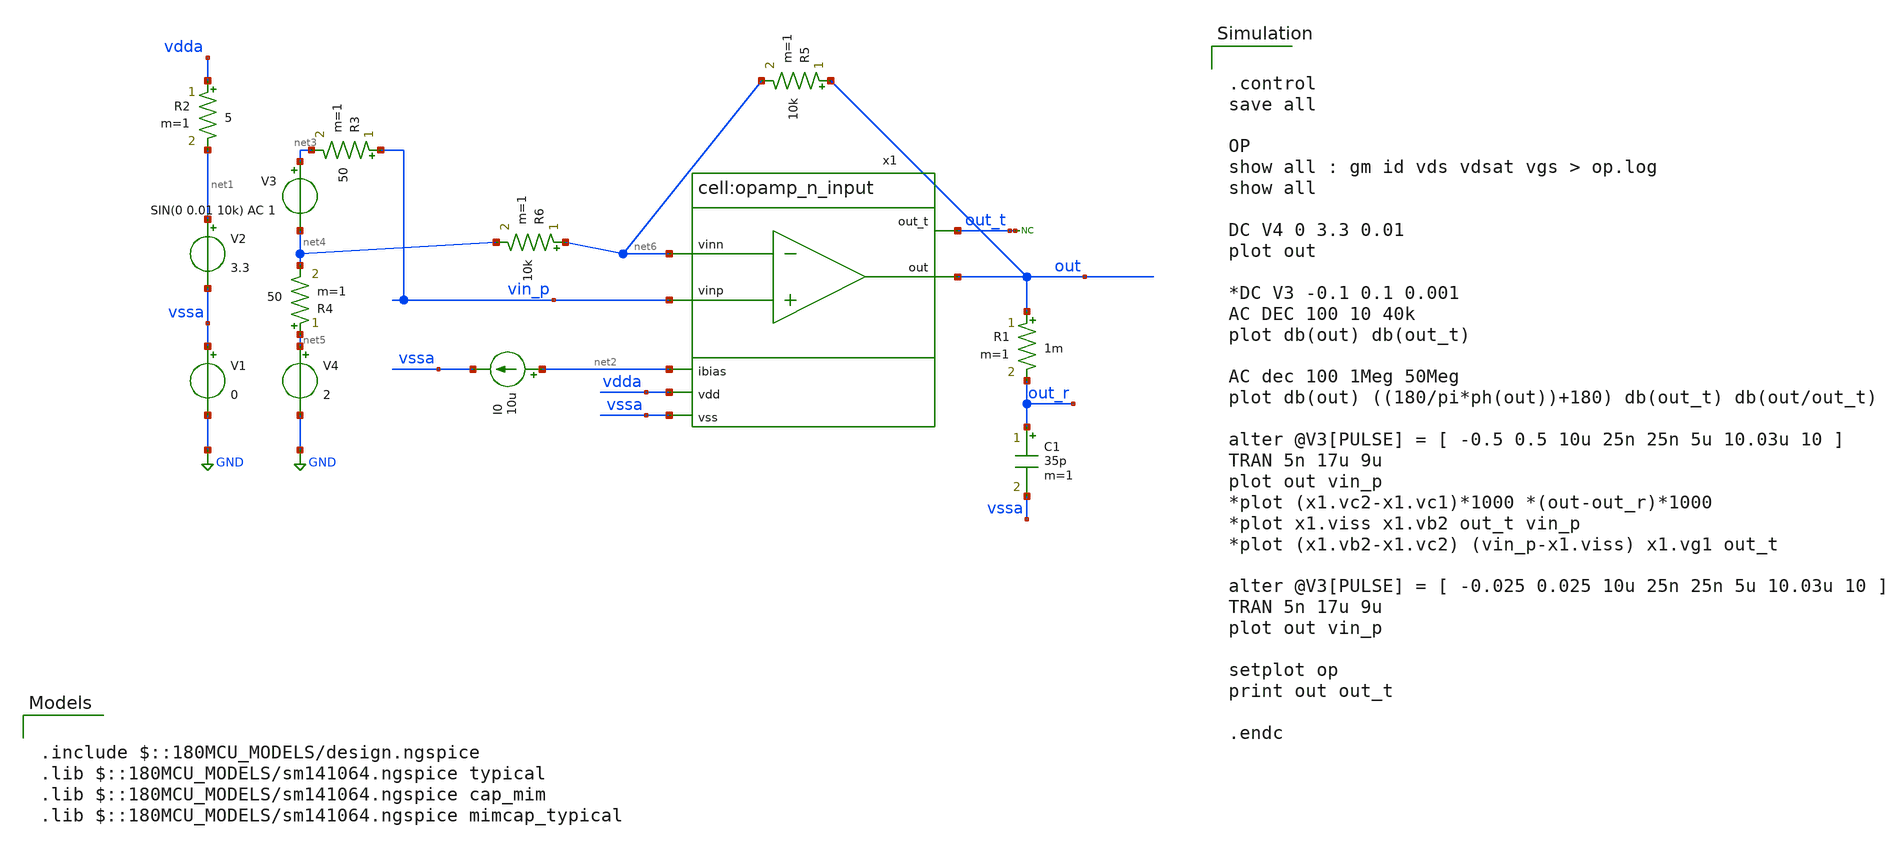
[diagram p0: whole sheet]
** sch_path: designs/libs/tb_analog/opamp/opamp_n_tb.sch
**.subckt opamp_n_tb
x1 vin_p net6 net2 vdda out vssa out_t opamp_n_input
V1 vssa GND 0
V2 net1 vssa 3.3
I0 net2 vssa 10u
V3 net3 net4 SIN(0 0.01 10k) AC 1
V4 net5 GND 2
C1 out_r vssa 35p m=1
* noconn out_t
R1 out out_r 1m m=1
R2 vdda net1 5 m=1
R3 vin_p net3 50 m=1
R4 net5 net4 50 m=1
R5 out net6 10k m=1
R6 net6 net4 10k m=1
**** begin user architecture code


.control
save all

OP
show all : gm id vds vdsat vgs > op.log
show all

DC V4 0 3.3 0.01
plot out

*DC V3 -0.1 0.1 0.001
AC DEC 100 10 40k
plot db(out) db(out_t)

AC dec 100 1Meg 50Meg
plot db(out) ((180/pi*ph(out))+180) db(out_t) db(out/out_t)

alter @V3[PULSE] = [ -0.5 0.5 10u 25n 25n 5u 10.03u 10 ]
TRAN 5n 17u 9u
plot out vin_p
*plot (x1.vc2-x1.vc1)*1000 *(out-out_r)*1000
*plot x1.viss x1.vb2 out_t vin_p
*plot (x1.vb2-x1.vc2) (vin_p-x1.viss) x1.vg1 out_t

alter @V3[PULSE] = [ -0.025 0.025 10u 25n 25n 5u 10.03u 10 ]
TRAN 5n 17u 9u
plot out vin_p

setplot op
print out out_t

.endc



.include $::180MCU_MODELS/design.ngspice
.lib $::180MCU_MODELS/sm141064.ngspice typical
.lib $::180MCU_MODELS/sm141064.ngspice cap_mim
.lib $::180MCU_MODELS/sm141064.ngspice mimcap_typical

**** end user architecture code
**.ends

* expanding   symbol:  libs/core_analog/opamp/opamp_n_input.sym # of pins=7
** sym_path: designs/libs/core_analog/opamp/opamp_n_input.sym
** sch_path: designs/libs/core_analog/opamp/opamp_n_input.sch
.subckt opamp_n_input vinp vinn ibias vdd out vss out_t
*.opin out
*.ipin vdd
*.ipin vss
*.ipin vinn
*.ipin ibias
*.ipin vinp
*.opin out_t
XM1 net1 vinn viss vss nfet_03v3 L=1u W=3u nf=1 ad='int((nf+1)/2) * W/nf * 0.18u' as='int((nf+2)/2) * W/nf * 0.18u'
+ pd='2*int((nf+1)/2) * (W/nf + 0.18u)' ps='2*int((nf+2)/2) * (W/nf + 0.18u)' nrd='0.18u / W' nrs='0.18u / W'
+ sa=0 sb=0 sd=0 m=1
XM2 net2 vinp viss vss nfet_03v3 L=1u W=3u nf=1 ad='int((nf+1)/2) * W/nf * 0.18u' as='int((nf+2)/2) * W/nf * 0.18u'
+ pd='2*int((nf+1)/2) * (W/nf + 0.18u)' ps='2*int((nf+2)/2) * (W/nf + 0.18u)' nrd='0.18u / W' nrs='0.18u / W'
+ sa=0 sb=0 sd=0 m=1
XM6 out_t vg1 vdd vdd pfet_03v3 L=1u W=5u nf=1 ad='int((nf+1)/2) * W/nf * 0.18u' as='int((nf+2)/2) * W/nf * 0.18u'
+ pd='2*int((nf+1)/2) * (W/nf + 0.18u)' ps='2*int((nf+2)/2) * (W/nf + 0.18u)' nrd='0.18u / W' nrs='0.18u / W'
+ sa=0 sb=0 sd=0 m=3
XM5 vg1 vg1 vdd vdd pfet_03v3 L=1u W=5u nf=1 ad='int((nf+1)/2) * W/nf * 0.18u' as='int((nf+2)/2) * W/nf * 0.18u'
+ pd='2*int((nf+1)/2) * (W/nf + 0.18u)' ps='2*int((nf+2)/2) * (W/nf + 0.18u)' nrd='0.18u / W' nrs='0.18u / W'
+ sa=0 sb=0 sd=0 m=3
XM4 out_t vb2 net2 vss nfet_03v3 L=0.6u W=5u nf=1 ad='int((nf+1)/2) * W/nf * 0.18u' as='int((nf+2)/2) * W/nf * 0.18u'
+ pd='2*int((nf+1)/2) * (W/nf + 0.18u)' ps='2*int((nf+2)/2) * (W/nf + 0.18u)' nrd='0.18u / W' nrs='0.18u / W'
+ sa=0 sb=0 sd=0 m=4
XM3 vg1 vb2 net1 vss nfet_03v3 L=0.6u W=5u nf=1 ad='int((nf+1)/2) * W/nf * 0.18u' as='int((nf+2)/2) * W/nf * 0.18u'
+ pd='2*int((nf+1)/2) * (W/nf + 0.18u)' ps='2*int((nf+2)/2) * (W/nf + 0.18u)' nrd='0.18u / W' nrs='0.18u / W'
+ sa=0 sb=0 sd=0 m=4
XM7 viss net3 vss vss nfet_03v3 L=2u W=4.5u nf=1 ad='int((nf+1)/2) * W/nf * 0.18u' as='int((nf+2)/2) * W/nf * 0.18u'
+ pd='2*int((nf+1)/2) * (W/nf + 0.18u)' ps='2*int((nf+2)/2) * (W/nf + 0.18u)' nrd='0.18u / W' nrs='0.18u / W'
+ sa=0 sb=0 sd=0 m=3
XM11 net3 net3 vss vss nfet_03v3 L=2u W=4.5u nf=1 ad='int((nf+1)/2) * W/nf * 0.18u' as='int((nf+2)/2) * W/nf * 0.18u'
+ pd='2*int((nf+1)/2) * (W/nf + 0.18u)' ps='2*int((nf+2)/2) * (W/nf + 0.18u)' nrd='0.18u / W' nrs='0.18u / W'
+ sa=0 sb=0 sd=0 m=1
x1 vdd vdd net4 net4 unit_pmos M=1
x2 vdd vdd net4 net5 unit_pmos M=1
x4 vdd vdd net4 vb2 unit_pmos M=1
x3 net4 vdd ibias ibias unit_pmos M=1
x5 net5 vdd ibias net6 unit_pmos M=1
XM10 vb2 vb2 viss vss nfet_03v3 L=4u W=2u nf=1 ad='int((nf+1)/2) * W/nf * 0.18u' as='int((nf+2)/2) * W/nf * 0.18u'
+ pd='2*int((nf+1)/2) * (W/nf + 0.18u)' ps='2*int((nf+2)/2) * (W/nf + 0.18u)' nrd='0.18u / W' nrs='0.18u / W'
+ sa=0 sb=0 sd=0 m=1
C1 out net2 2p m=1
XM8 out net3 vss vss nfet_03v3 L=0.8u W=5.5u nf=1 ad='int((nf+1)/2) * W/nf * 0.18u' as='int((nf+2)/2) * W/nf * 0.18u'
+ pd='2*int((nf+1)/2) * (W/nf + 0.18u)' ps='2*int((nf+2)/2) * (W/nf + 0.18u)' nrd='0.18u / W' nrs='0.18u / W'
+ sa=0 sb=0 sd=0 m=2
XM9 out out_t vdd vdd pfet_03v3 L=0.8u W=4.5u nf=1 ad='int((nf+1)/2) * W/nf * 0.18u' as='int((nf+2)/2) * W/nf * 0.18u'
+ pd='2*int((nf+1)/2) * (W/nf + 0.18u)' ps='2*int((nf+2)/2) * (W/nf + 0.18u)' nrd='0.18u / W' nrs='0.18u / W'
+ sa=0 sb=0 sd=0 m=15
XM12 net6 net6 net3 vss nfet_03v3 L=2u W=4.5u nf=1 ad='int((nf+1)/2) * W/nf * 0.18u' as='int((nf+2)/2) * W/nf * 0.18u'
+ pd='2*int((nf+1)/2) * (W/nf + 0.18u)' ps='2*int((nf+2)/2) * (W/nf + 0.18u)' nrd='0.18u / W' nrs='0.18u / W'
+ sa=0 sb=0 sd=0 m=1
.ends


* expanding   symbol:  libs/core_analog/unit_pmos/unit_pmos.sym # of pins=4
** sym_path: libs/core_analog/unit_pmos/unit_pmos.sym
** sch_path: libs/core_analog/unit_pmos/unit_pmos.sch
.subckt unit_pmos drain sub gate source
*.iopin drain
*.iopin source
*.iopin sub
*.iopin gate
**** begin user architecture code

.param M=1

**** end user architecture code
XM3 drain gate source sub pfet_03v3 L=1u W=3.5u nf=1 ad='int((nf+1)/2) * W/nf * 0.18u' as='int((nf+2)/2) * W/nf * 0.18u'
+ pd='2*int((nf+1)/2) * (W/nf + 0.18u)' ps='2*int((nf+2)/2) * (W/nf + 0.18u)' nrd='0.18u / W' nrs='0.18u / W'
+ sa=0 sb=0 sd=0 m={M}
.ends

.GLOBAL GND
.end
